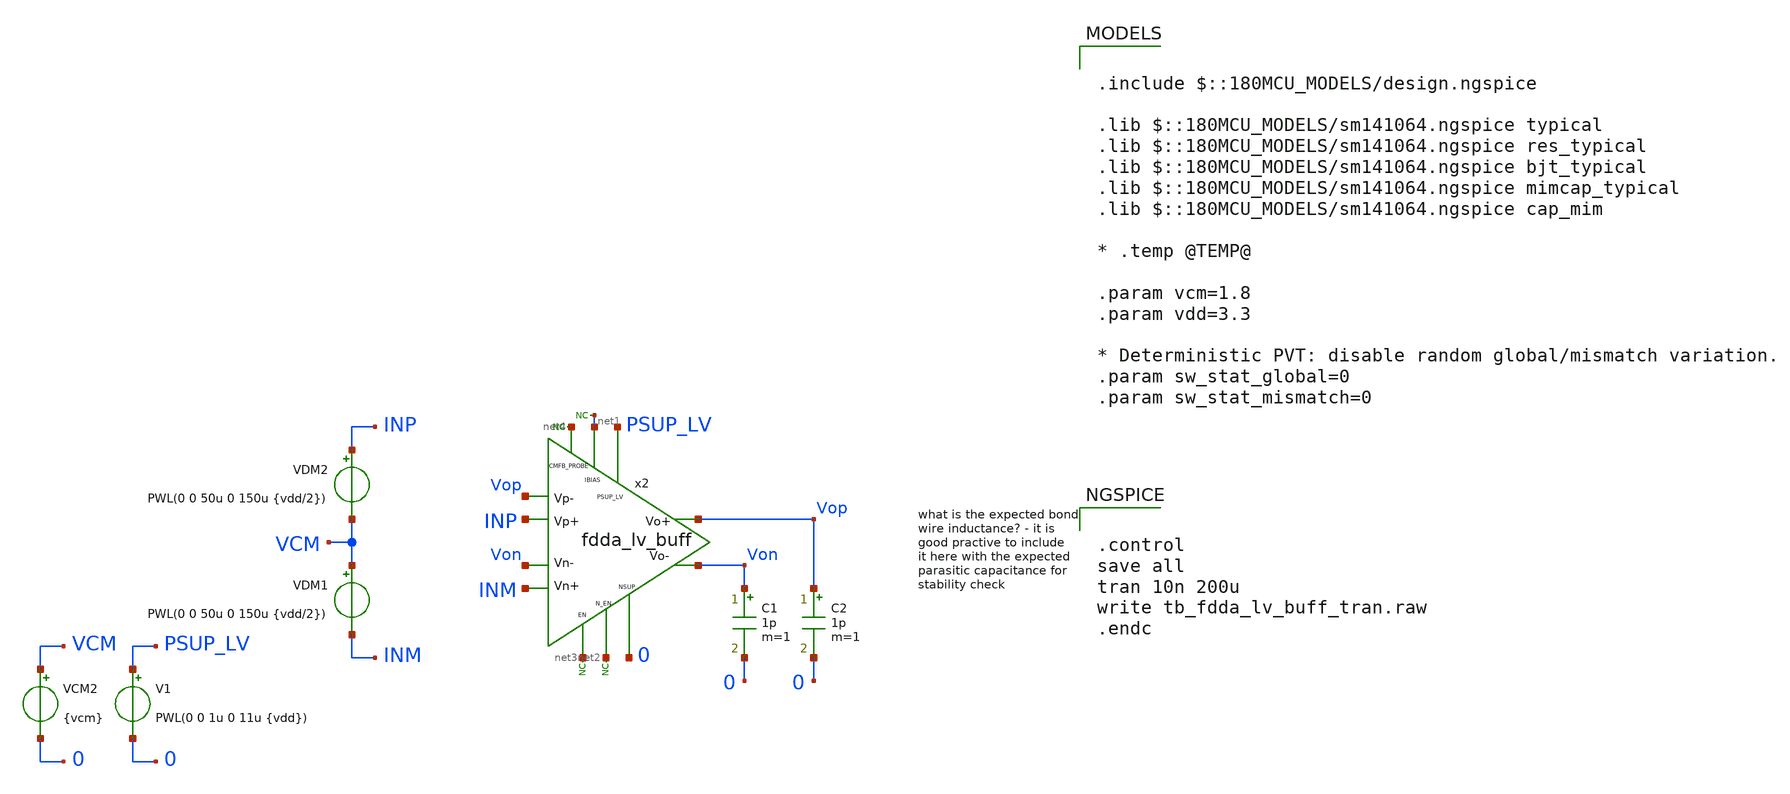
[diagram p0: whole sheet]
** sch_path: xschem/blocks/fdda_lv_buff/tb_fdda_lv_buff_tran.sch
**.subckt tb_fdda_lv_buff_tran
C1 Von 0 1p m=1
x2 PSUP_LV Vop Von INM INP Vop Von net1 net2 net3 0 net4 fdda_lv_buff
* noconn #net1
* noconn #net3
* noconn #net2
V1 PSUP_LV 0 PWL(0 0 1u 0 11u {vdd})
C2 Vop 0 1p m=1
VCM2 VCM 0 {vcm}
VDM2 INP VCM PWL(0 0 50u 0 150u {vdd/2})
VDM1 VCM INM PWL(0 0 50u 0 150u {vdd/2})
* noconn #net4
**** begin user architecture code

.include $::180MCU_MODELS/design.ngspice

.lib $::180MCU_MODELS/sm141064.ngspice typical
.lib $::180MCU_MODELS/sm141064.ngspice res_typical
.lib $::180MCU_MODELS/sm141064.ngspice bjt_typical
.lib $::180MCU_MODELS/sm141064.ngspice mimcap_typical
.lib $::180MCU_MODELS/sm141064.ngspice cap_mim

* .temp @TEMP@

.param vcm=1.8
.param vdd=3.3

* Deterministic PVT: disable random global/mismatch variation.
.param sw_stat_global=0
.param sw_stat_mismatch=0



.control
save all
tran 10n 200u
write tb_fdda_lv_buff_tran.raw
.endc


**** end user architecture code
**.ends
.end
